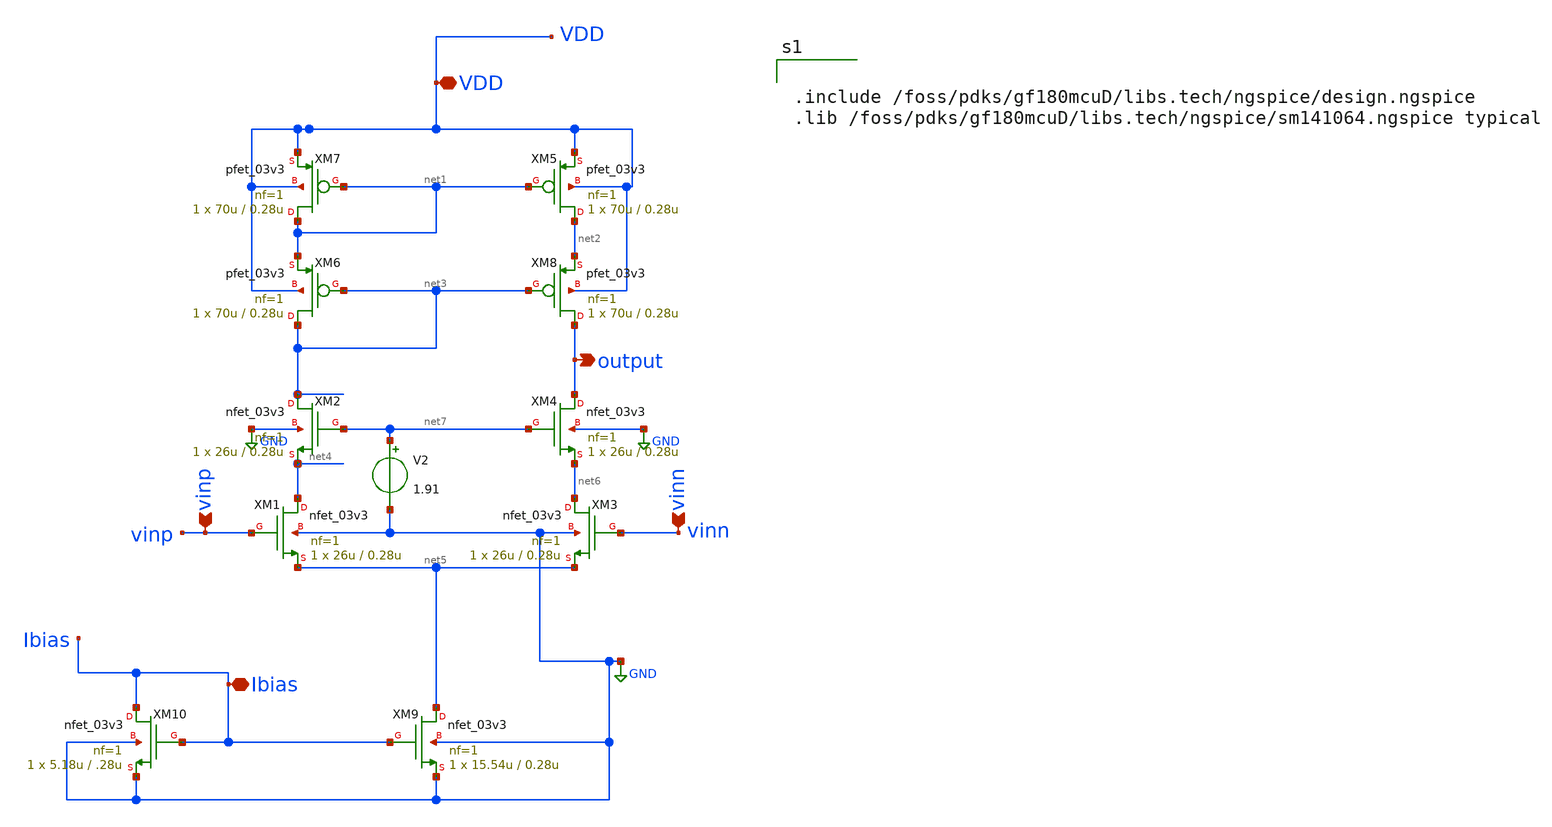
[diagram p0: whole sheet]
** sch_path: designs/libs/core_amps/ota_telescopic/telescopic_cascode.sch
**.subckt telescopic_cascode vinp vinn output Ibias VDD
*.ipin vinp
*.ipin vinn
*.opin output
*.iopin Ibias
*.iopin VDD
V2 net7 GND 1.91
XM8 output net3 net2 VDD pfet_03v3 L=0.28u W=70u nf=1 ad='int((nf+1)/2) * W/nf * 0.18u' as='int((nf+2)/2) * W/nf * 0.18u'
+ pd='2*int((nf+1)/2) * (W/nf + 0.18u)' ps='2*int((nf+2)/2) * (W/nf + 0.18u)' nrd='0.18u / W' nrs='0.18u / W'
+ sa=0 sb=0 sd=0 m=1
XM4 output net7 net6 GND nfet_03v3 L=0.28u W=26u nf=1 ad='int((nf+1)/2) * W/nf * 0.18u' as='int((nf+2)/2) * W/nf * 0.18u'
+ pd='2*int((nf+1)/2) * (W/nf + 0.18u)' ps='2*int((nf+2)/2) * (W/nf + 0.18u)' nrd='0.18u / W' nrs='0.18u / W'
+ sa=0 sb=0 sd=0 m=1
XM1 net4 vinp net5 GND nfet_03v3 L=0.28u W=26u nf=1 ad='int((nf+1)/2) * W/nf * 0.18u' as='int((nf+2)/2) * W/nf * 0.18u'
+ pd='2*int((nf+1)/2) * (W/nf + 0.18u)' ps='2*int((nf+2)/2) * (W/nf + 0.18u)' nrd='0.18u / W' nrs='0.18u / W'
+ sa=0 sb=0 sd=0 m=1
XM2 net3 net7 net4 GND nfet_03v3 L=0.28u W=26u nf=1 ad='int((nf+1)/2) * W/nf * 0.18u' as='int((nf+2)/2) * W/nf * 0.18u'
+ pd='2*int((nf+1)/2) * (W/nf + 0.18u)' ps='2*int((nf+2)/2) * (W/nf + 0.18u)' nrd='0.18u / W' nrs='0.18u / W'
+ sa=0 sb=0 sd=0 m=1
XM3 net6 vinn net5 GND nfet_03v3 L=0.28u W=26u nf=1 ad='int((nf+1)/2) * W/nf * 0.18u' as='int((nf+2)/2) * W/nf * 0.18u'
+ pd='2*int((nf+1)/2) * (W/nf + 0.18u)' ps='2*int((nf+2)/2) * (W/nf + 0.18u)' nrd='0.18u / W' nrs='0.18u / W'
+ sa=0 sb=0 sd=0 m=1
XM5 net2 net1 VDD VDD pfet_03v3 L=0.28u W=70u nf=1 ad='int((nf+1)/2) * W/nf * 0.18u' as='int((nf+2)/2) * W/nf * 0.18u'
+ pd='2*int((nf+1)/2) * (W/nf + 0.18u)' ps='2*int((nf+2)/2) * (W/nf + 0.18u)' nrd='0.18u / W' nrs='0.18u / W'
+ sa=0 sb=0 sd=0 m=1
XM6 net3 net3 net1 VDD pfet_03v3 L=0.28u W=70u nf=1 ad='int((nf+1)/2) * W/nf * 0.18u' as='int((nf+2)/2) * W/nf * 0.18u'
+ pd='2*int((nf+1)/2) * (W/nf + 0.18u)' ps='2*int((nf+2)/2) * (W/nf + 0.18u)' nrd='0.18u / W' nrs='0.18u / W'
+ sa=0 sb=0 sd=0 m=1
XM7 net1 net1 VDD VDD pfet_03v3 L=0.28u W=70u nf=1 ad='int((nf+1)/2) * W/nf * 0.18u' as='int((nf+2)/2) * W/nf * 0.18u'
+ pd='2*int((nf+1)/2) * (W/nf + 0.18u)' ps='2*int((nf+2)/2) * (W/nf + 0.18u)' nrd='0.18u / W' nrs='0.18u / W'
+ sa=0 sb=0 sd=0 m=1
XM9 net5 Ibias GND GND nfet_03v3 L=0.28u W=15.54u nf=1 ad='int((nf+1)/2) * W/nf * 0.18u' as='int((nf+2)/2) * W/nf * 0.18u'
+ pd='2*int((nf+1)/2) * (W/nf + 0.18u)' ps='2*int((nf+2)/2) * (W/nf + 0.18u)' nrd='0.18u / W' nrs='0.18u / W'
+ sa=0 sb=0 sd=0 m=1
XM10 Ibias Ibias GND GND nfet_03v3 L=.28u W=5.18u nf=1 ad='int((nf+1)/2) * W/nf * 0.18u' as='int((nf+2)/2) * W/nf * 0.18u'
+ pd='2*int((nf+1)/2) * (W/nf + 0.18u)' ps='2*int((nf+2)/2) * (W/nf + 0.18u)' nrd='0.18u / W' nrs='0.18u / W'
+ sa=0 sb=0 sd=0 m=1
**** begin user architecture code


.include /foss/pdks/gf180mcuD/libs.tech/ngspice/design.ngspice
.lib /foss/pdks/gf180mcuD/libs.tech/ngspice/sm141064.ngspice typical

**** end user architecture code
**.ends
.GLOBAL GND
.end
